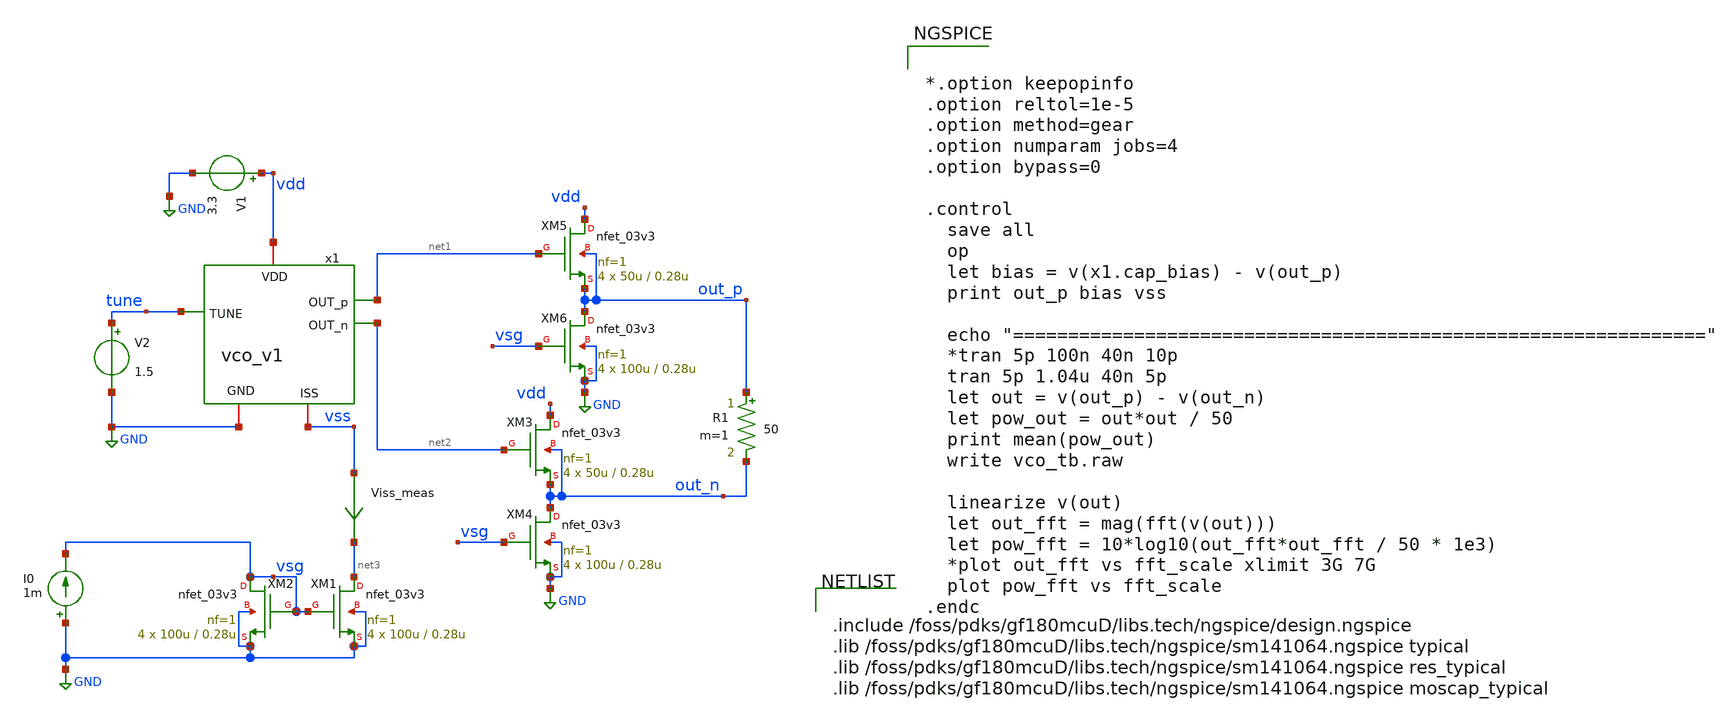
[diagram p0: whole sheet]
** sch_path: team_src/xschem/vco_tb.sch
**.subckt vco_tb
R1 out_p out_n 50 m=1
V1 vdd GND 3.3
.save i(v1)
x1 vdd net1 net2 GND tune vss vco_v1
V2 tune GND 1.5
.save i(v2)
XM2 vsg vsg GND GND nfet_03v3 L=0.28u W=100u nf=1 ad='int((nf+1)/2) * W/nf * 0.18u' as='int((nf+2)/2) * W/nf * 0.18u'
+ pd='2*int((nf+1)/2) * (W/nf + 0.18u)' ps='2*int((nf+2)/2) * (W/nf + 0.18u)' nrd='0.18u / W' nrs='0.18u / W'
+ sa=0 sb=0 sd=0 m=4
XM1 net3 vsg GND GND nfet_03v3 L=0.28u W=100u nf=1 ad='int((nf+1)/2) * W/nf * 0.18u' as='int((nf+2)/2) * W/nf * 0.18u'
+ pd='2*int((nf+1)/2) * (W/nf + 0.18u)' ps='2*int((nf+2)/2) * (W/nf + 0.18u)' nrd='0.18u / W' nrs='0.18u / W'
+ sa=0 sb=0 sd=0 m=4
Viss_meas vss net3 0
.save i(viss_meas)
I0 GND vsg 1m
XM3 vdd net2 out_n out_n nfet_03v3 L=0.28u W=50u nf=1 ad='int((nf+1)/2) * W/nf * 0.18u' as='int((nf+2)/2) * W/nf * 0.18u'
+ pd='2*int((nf+1)/2) * (W/nf + 0.18u)' ps='2*int((nf+2)/2) * (W/nf + 0.18u)' nrd='0.18u / W' nrs='0.18u / W'
+ sa=0 sb=0 sd=0 m=4
XM4 out_n vsg GND GND nfet_03v3 L=0.28u W=100u nf=1 ad='int((nf+1)/2) * W/nf * 0.18u' as='int((nf+2)/2) * W/nf * 0.18u'
+ pd='2*int((nf+1)/2) * (W/nf + 0.18u)' ps='2*int((nf+2)/2) * (W/nf + 0.18u)' nrd='0.18u / W' nrs='0.18u / W'
+ sa=0 sb=0 sd=0 m=4
XM5 vdd net1 out_p out_p nfet_03v3 L=0.28u W=50u nf=1 ad='int((nf+1)/2) * W/nf * 0.18u' as='int((nf+2)/2) * W/nf * 0.18u'
+ pd='2*int((nf+1)/2) * (W/nf + 0.18u)' ps='2*int((nf+2)/2) * (W/nf + 0.18u)' nrd='0.18u / W' nrs='0.18u / W'
+ sa=0 sb=0 sd=0 m=4
XM6 out_p vsg GND GND nfet_03v3 L=0.28u W=100u nf=1 ad='int((nf+1)/2) * W/nf * 0.18u' as='int((nf+2)/2) * W/nf * 0.18u'
+ pd='2*int((nf+1)/2) * (W/nf + 0.18u)' ps='2*int((nf+2)/2) * (W/nf + 0.18u)' nrd='0.18u / W' nrs='0.18u / W'
+ sa=0 sb=0 sd=0 m=4
**** begin user architecture code


*.option keepopinfo
.option reltol=1e-5
.option method=gear
.option numparam jobs=4
.option bypass=0

.control
  save all
  op
  let bias = v(x1.cap_bias) - v(out_p)
  print out_p bias vss

  echo "==============================================================="
  *tran 5p 100n 40n 10p
  tran 5p 1.04u 40n 5p
  let out = v(out_p) - v(out_n)
  let pow_out = out*out / 50
  print mean(pow_out)
  write vco_tb.raw

  linearize v(out)
  let out_fft = mag(fft(v(out)))
  let pow_fft = 10*log10(out_fft*out_fft / 50 * 1e3)
  *plot out_fft vs fft_scale xlimit 3G 7G
  plot pow_fft vs fft_scale
.endc




.include /foss/pdks/gf180mcuD/libs.tech/ngspice/design.ngspice
.lib /foss/pdks/gf180mcuD/libs.tech/ngspice/sm141064.ngspice typical
.lib /foss/pdks/gf180mcuD/libs.tech/ngspice/sm141064.ngspice res_typical
.lib /foss/pdks/gf180mcuD/libs.tech/ngspice/sm141064.ngspice moscap_typical


**** end user architecture code
**.ends

* expanding   symbol:  vco_v1.sym # of pins=6
** sym_path: team_src/xschem/vco_v1.sym
** sch_path: team_src/xschem/vco_v1.sch
.subckt vco_v1 VDD OUT_p OUT_n GND TUNE ISS
*.iopin VDD
*.iopin ISS
*.iopin GND
*.ipin TUNE
*.opin OUT_p
*.opin OUT_n
XM1 OUT_p OUT_n ISS ISS nfet_03v3 L=0.28u W=40u nf=1 ad='int((nf+1)/2) * W/nf * 0.18u' as='int((nf+2)/2) * W/nf * 0.18u'
+ pd='2*int((nf+1)/2) * (W/nf + 0.18u)' ps='2*int((nf+2)/2) * (W/nf + 0.18u)' nrd='0.18u / W' nrs='0.18u / W'
+ sa=0 sb=0 sd=0 m=1
XM2 OUT_p OUT_n VDD VDD pfet_03v3 L=0.28u W=70u nf=1 ad='int((nf+1)/2) * W/nf * 0.18u' as='int((nf+2)/2) * W/nf * 0.18u'
+ pd='2*int((nf+1)/2) * (W/nf + 0.18u)' ps='2*int((nf+2)/2) * (W/nf + 0.18u)' nrd='0.18u / W' nrs='0.18u / W'
+ sa=0 sb=0 sd=0 m=1
X1 OUT_n OUT_p GND vco_inductor_v2
XM3 OUT_n OUT_p VDD VDD pfet_03v3 L=0.28u W=70u nf=1 ad='int((nf+1)/2) * W/nf * 0.18u' as='int((nf+2)/2) * W/nf * 0.18u'
+ pd='2*int((nf+1)/2) * (W/nf + 0.18u)' ps='2*int((nf+2)/2) * (W/nf + 0.18u)' nrd='0.18u / W' nrs='0.18u / W'
+ sa=0 sb=0 sd=0 m=1
XM4 OUT_n OUT_p ISS ISS nfet_03v3 L=0.28u W=40u nf=1 ad='int((nf+1)/2) * W/nf * 0.18u' as='int((nf+2)/2) * W/nf * 0.18u'
+ pd='2*int((nf+1)/2) * (W/nf + 0.18u)' ps='2*int((nf+2)/2) * (W/nf + 0.18u)' nrd='0.18u / W' nrs='0.18u / W'
+ sa=0 sb=0 sd=0 m=1
XC1 cap_bias OUT_n cap_nmos_03v3_b c_width=5u c_length=5u m=21
XC4 cap_bias OUT_p cap_nmos_03v3_b c_width=5u c_length=5u m=21
XR2 TUNE cap_bias GND ppolyf_u_3k r_width=1u r_length=5u m=1
.ends


* expanding   symbol:  vco_inductor_v2.sym # of pins=3
** sym_path: team_src/xschem/vco_inductor_v2.sym
.include $UPRJ_ROOT/team_src/xschem/vco_inductor_v2.subckt
.GLOBAL GND
.end
